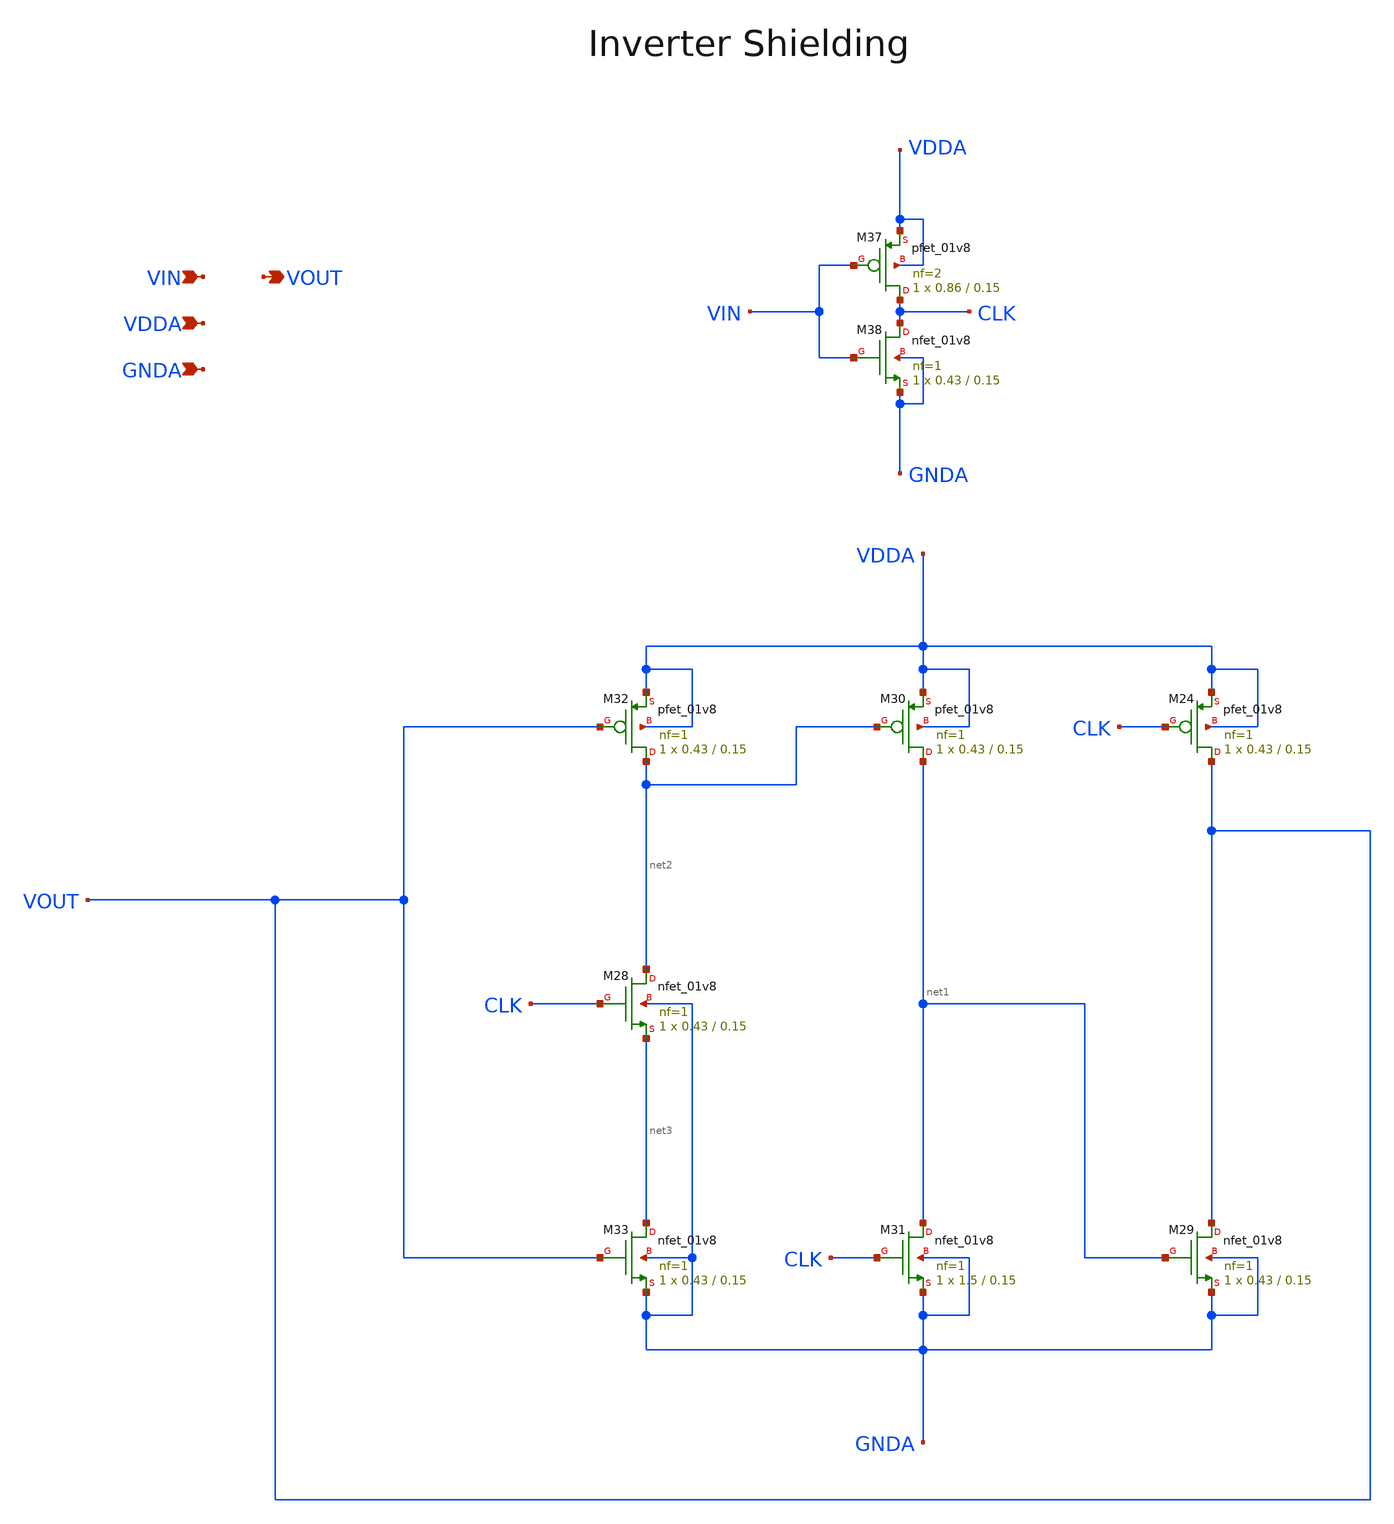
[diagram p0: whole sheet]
** sch_path: projects/pll/divider/xschem_ngspice/TSPC_FF_ratioed_divide2_2.sch
**.subckt TSPC_FF_ratioed_divide2_2 VIN VOUT VDDA GNDA
*.ipin VIN
*.opin VOUT
*.ipin VDDA
*.ipin GNDA
XM24 VOUT CLK VDDA VDDA sky130_fd_pr__pfet_01v8 L=0.15 W=0.43 nf=1 ad='int((nf+1)/2) * W/nf * 0.29' as='int((nf+2)/2) * W/nf * 0.29'
+ pd='2*int((nf+1)/2) * (W/nf + 0.29)' ps='2*int((nf+2)/2) * (W/nf + 0.29)' nrd='0.29 / W' nrs='0.29 / W'
+ sa=0 sb=0 sd=0 mult=1 m=1
XM29 VOUT net1 GNDA GNDA sky130_fd_pr__nfet_01v8 L=0.15 W=0.43 nf=1 ad='int((nf+1)/2) * W/nf * 0.29'
+ as='int((nf+2)/2) * W/nf * 0.29' pd='2*int((nf+1)/2) * (W/nf + 0.29)' ps='2*int((nf+2)/2) * (W/nf + 0.29)'
+ nrd='0.29 / W' nrs='0.29 / W' sa=0 sb=0 sd=0 mult=1 m=1
XM30 net1 net2 VDDA VDDA sky130_fd_pr__pfet_01v8 L=0.15 W=0.43 nf=1 ad='int((nf+1)/2) * W/nf * 0.29'
+ as='int((nf+2)/2) * W/nf * 0.29' pd='2*int((nf+1)/2) * (W/nf + 0.29)' ps='2*int((nf+2)/2) * (W/nf + 0.29)'
+ nrd='0.29 / W' nrs='0.29 / W' sa=0 sb=0 sd=0 mult=1 m=1
XM31 net1 CLK GNDA GNDA sky130_fd_pr__nfet_01v8 L=0.15 W=1.5 nf=1 ad='int((nf+1)/2) * W/nf * 0.29' as='int((nf+2)/2) * W/nf * 0.29'
+ pd='2*int((nf+1)/2) * (W/nf + 0.29)' ps='2*int((nf+2)/2) * (W/nf + 0.29)' nrd='0.29 / W' nrs='0.29 / W'
+ sa=0 sb=0 sd=0 mult=1 m=1
XM32 net2 VOUT VDDA VDDA sky130_fd_pr__pfet_01v8 L=0.15 W=0.43 nf=1 ad='int((nf+1)/2) * W/nf * 0.29'
+ as='int((nf+2)/2) * W/nf * 0.29' pd='2*int((nf+1)/2) * (W/nf + 0.29)' ps='2*int((nf+2)/2) * (W/nf + 0.29)'
+ nrd='0.29 / W' nrs='0.29 / W' sa=0 sb=0 sd=0 mult=1 m=1
XM33 net3 VOUT GNDA GNDA sky130_fd_pr__nfet_01v8 L=0.15 W=0.43 nf=1 ad='int((nf+1)/2) * W/nf * 0.29'
+ as='int((nf+2)/2) * W/nf * 0.29' pd='2*int((nf+1)/2) * (W/nf + 0.29)' ps='2*int((nf+2)/2) * (W/nf + 0.29)'
+ nrd='0.29 / W' nrs='0.29 / W' sa=0 sb=0 sd=0 mult=1 m=1
XM28 net2 CLK net3 GNDA sky130_fd_pr__nfet_01v8 L=0.15 W=0.43 nf=1 ad='int((nf+1)/2) * W/nf * 0.29' as='int((nf+2)/2) * W/nf * 0.29'
+ pd='2*int((nf+1)/2) * (W/nf + 0.29)' ps='2*int((nf+2)/2) * (W/nf + 0.29)' nrd='0.29 / W' nrs='0.29 / W'
+ sa=0 sb=0 sd=0 mult=1 m=1
XM37 CLK VIN VDDA VDDA sky130_fd_pr__pfet_01v8 L=0.15 W=0.86 nf=2 ad='int((nf+1)/2) * W/nf * 0.29' as='int((nf+2)/2) * W/nf * 0.29'
+ pd='2*int((nf+1)/2) * (W/nf + 0.29)' ps='2*int((nf+2)/2) * (W/nf + 0.29)' nrd='0.29 / W' nrs='0.29 / W'
+ sa=0 sb=0 sd=0 mult=1 m=1
XM38 CLK VIN GNDA GNDA sky130_fd_pr__nfet_01v8 L=0.15 W=0.43 nf=1 ad='int((nf+1)/2) * W/nf * 0.29' as='int((nf+2)/2) * W/nf * 0.29'
+ pd='2*int((nf+1)/2) * (W/nf + 0.29)' ps='2*int((nf+2)/2) * (W/nf + 0.29)' nrd='0.29 / W' nrs='0.29 / W'
+ sa=0 sb=0 sd=0 mult=1 m=1
**.ends
.end
